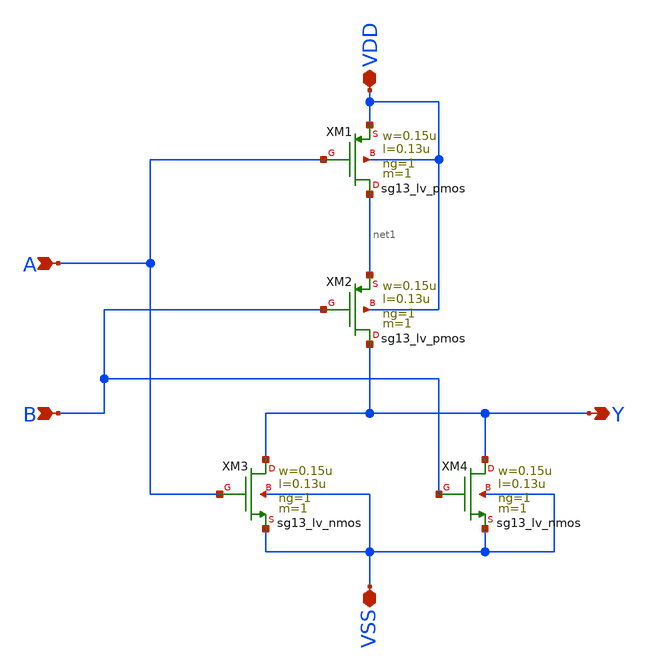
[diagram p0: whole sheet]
** sch_path: LogicGate/NOR2.sch
**.subckt NOR2 A B Y VDD VSS
*.ipin A
*.ipin B
*.opin Y
*.iopin VDD
*.iopin VSS
XXM1 net1 A VDD VDD sg13_lv_pmos w=0.15u l=0.13u ng=1 m=1 mm_ok=1
XXM2 Y B net1 VDD sg13_lv_pmos w=0.15u l=0.13u ng=1 m=1 mm_ok=1
XXM3 Y A VSS VSS sg13_lv_nmos w=0.15u l=0.13u ng=1 m=1 mm_ok=1
XXM4 Y B VSS VSS sg13_lv_nmos w=0.15u l=0.13u ng=1 m=1 mm_ok=1
**.ends
.end
